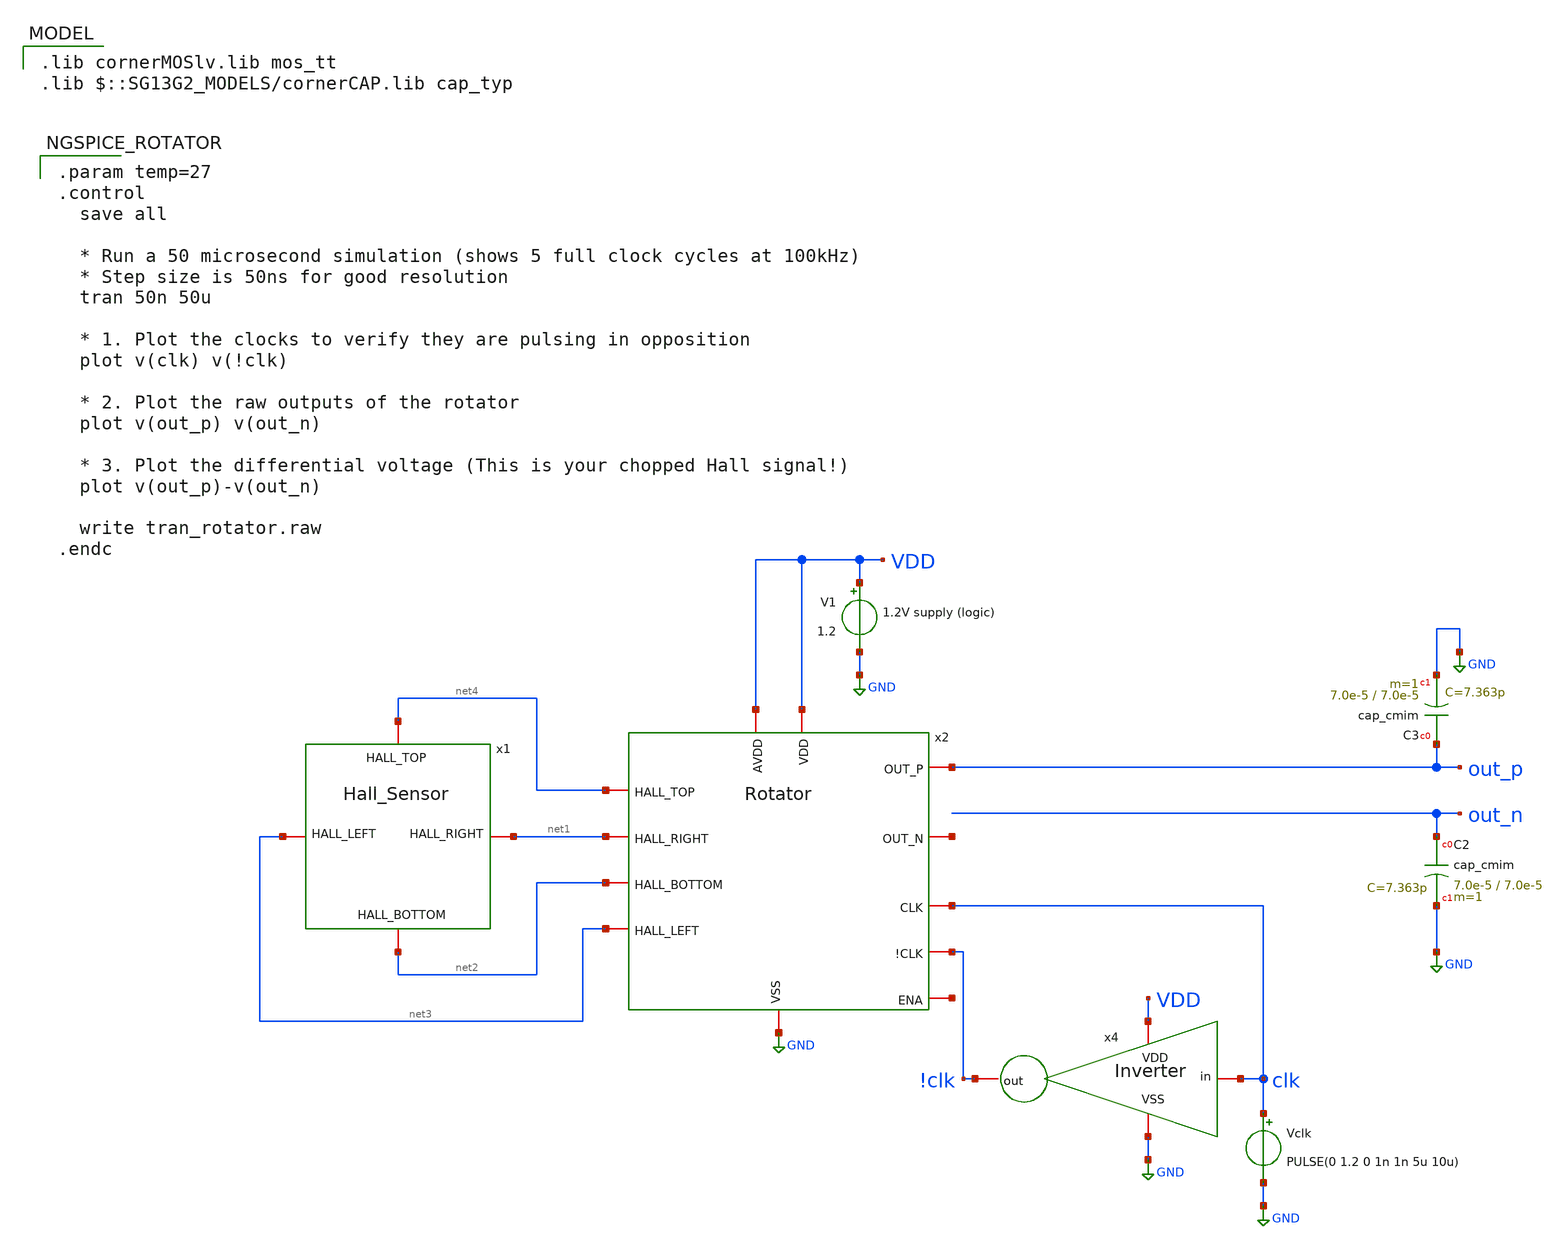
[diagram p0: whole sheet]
** sch_path: xschem/Rotator_Testbench.sch
**.subckt Rotator_Testbench
x1 net4 net3 net1 net2 Hall_Sensor
x2 VDD GND clk !clk net4 out_p net3 net1 net2 net5 VDD net6 Rotator
V1 VDD GND 1.2
XC2 out_n GND cap_cmim w=7.0e-5 l=7.0e-5 m=1 mm_ok=1
XC3 out_p GND cap_cmim w=7.0e-5 l=7.0e-5 m=1 mm_ok=1
Vclk clk GND PULSE(0 1.2 0 1n 1n 5u 10u)
x4 VDD clk !clk GND Inverter
**** begin user architecture code
 .lib cornerMOSlv.lib mos_tt
.lib $::SG13G2_MODELS/cornerCAP.lib cap_typ


.param temp=27
.control
  save all

  * Run a 50 microsecond simulation (shows 5 full clock cycles at 100kHz)
  * Step size is 50ns for good resolution
  tran 50n 50u

  * 1. Plot the clocks to verify they are pulsing in opposition
  plot v(clk) v(!clk)

  * 2. Plot the raw outputs of the rotator
  plot v(out_p) v(out_n)

  * 3. Plot the differential voltage (This is your chopped Hall signal!)
  plot v(out_p)-v(out_n)

  write tran_rotator.raw
.endc


**** end user architecture code
**.ends

* expanding   symbol:  /headless/eda/Hall_Xschem_Logic/Hall_Sensor.sym # of pins=4
** sym_path: xschem/Hall_Sensor.sym
** sch_path: xschem/Hall_Sensor.sch
.subckt Hall_Sensor HALL_TOP HALL_LEFT HALL_RIGHT HALL_BOTTOM
*.iopin HALL_TOP
*.iopin HALL_BOTTOM
*.iopin HALL_LEFT
*.iopin HALL_RIGHT
R1 HALL_TOP HALL_LEFT 1k m=1
R2 HALL_TOP HALL_RIGHT 1k m=1
R3 HALL_LEFT HALL_BOTTOM 1k m=1
R4 HALL_RIGHT HALL_BOTTOM 1k m=1
**** begin user architecture code


* Dummy voltage representing the magnetic field (B_FIELD)
* We initialize it to 0. The testbench will alter this!
VB B_FIELD 0 0

* Phase 1: Bias flowing Top->Bottom creates a Hall current Left->Right
B_LR HALL_RIGHT HALL_LEFT I = V(HALL_TOP, HALL_BOTTOM) * V(B_FIELD) * 35e-6

* Phase 2: Bias flowing Left->Right creates a Hall current Top->Bottom
B_TB HALL_TOP HALL_BOTTOM I = V(HALL_LEFT, HALL_RIGHT) * V(B_FIELD) * 35e-6


**** end user architecture code
.ends


* expanding   symbol:  /headless/eda/Hall_Xschem_Logic/Rotator.sym # of pins=12
** sym_path: xschem/Rotator.sym
** sch_path: xschem/Rotator.sch
.subckt Rotator VDD VSS CLK !CLK HALL_TOP OUT_P HALL_LEFT HALL_RIGHT HALL_BOTTOM OUT_N AVDD ENA
*.iopin HALL_TOP
*.iopin HALL_RIGHT
*.iopin HALL_LEFT
*.iopin HALL_BOTTOM
*.iopin OUT_P
*.iopin OUT_N
*.iopin VDD
*.iopin VSS
*.iopin CLK
*.iopin !CLK
*.iopin AVDD
*.iopin ENA
x10 CLK VDD HALL_TOP OUT_P VSS !CLK CMOS_transmission_gate
XM7 HALL_BOTTOM CLK VSS VSS sg13_lv_nmos w=5u l=0.13u ng=3 m=1 mm_ok=1
XM1 HALL_LEFT !CLK VSS VSS sg13_lv_nmos w=5u l=0.13u ng=3 m=1 mm_ok=1
XM5 HALL_RIGHT CLK net1 VDD sg13_lv_pmos w=10u l=0.13u ng=3 m=1 mm_ok=1
XM2 HALL_TOP !CLK net2 VDD sg13_lv_pmos w=10u l=0.13u ng=3 m=1 mm_ok=1
x1 !CLK VDD HALL_RIGHT OUT_N VSS CLK CMOS_transmission_gate
x2 !CLK VDD HALL_LEFT OUT_P VSS CLK CMOS_transmission_gate
x3 CLK VDD HALL_BOTTOM OUT_N VSS !CLK CMOS_transmission_gate
XM3 net2 ENA AVDD VDD sg13_lv_pmos w=10u l=0.13u ng=3 m=1 mm_ok=1
XM4 net1 ENA AVDD VDD sg13_lv_pmos w=10u l=0.13u ng=3 m=1 mm_ok=1
.ends


* expanding   symbol:  /headless/eda/Hall_Xschem_Logic/Inverter.sym # of pins=4
** sym_path: xschem/Inverter.sym
** sch_path: xschem/Inverter.sch
.subckt Inverter VDD in out VSS
*.iopin VDD
*.iopin VSS
*.iopin in
*.iopin out
XM1 out in VSS VSS sg13_lv_nmos w=1u l=0.13u ng=1 m=1 mm_ok=1
XM2 out in VDD VDD sg13_lv_pmos w=2u l=0.13u ng=1 m=1 mm_ok=1
.ends


* expanding   symbol:  /headless/eda/Hall_Xschem_Logic/CMOS_transmission_gate.sym # of pins=6
** sym_path: xschem/CMOS_transmission_gate.sym
** sch_path: xschem/CMOS_transmission_gate.sch
.subckt CMOS_transmission_gate !Control vdd Vin Vout gnd Control
*.iopin Vout
*.iopin Vin
*.iopin !Control
*.iopin Control
*.iopin gnd
*.iopin vdd
XM1 Vin Control Vout gnd sg13_lv_nmos w=0.5u l=0.13u ng=1 m=1 mm_ok=1
XM2 Vin !Control Vout vdd sg13_lv_pmos w=1u l=0.13u ng=1 m=1 mm_ok=1
.ends

.GLOBAL GND
.end
